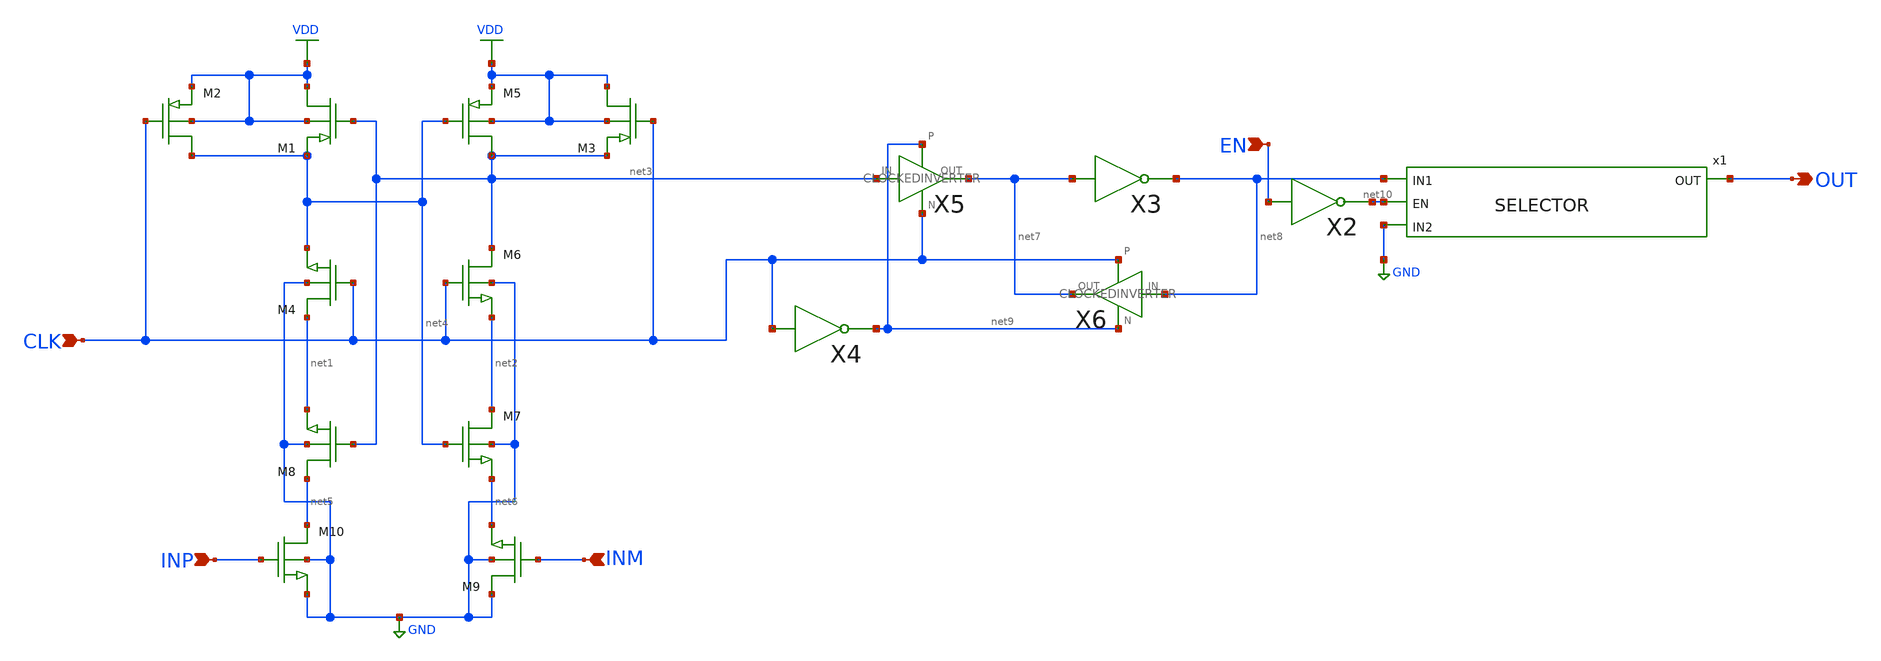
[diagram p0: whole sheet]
** sch_path: clocked_comparatorDF2.sch
**.subckt clocked_comparatorDF2 INP INM CLK OUT EN
*.ipin INP
*.ipin INM
*.ipin CLK
*.opin OUT
*.ipin EN
M4 net1 CLK net4 GND nch w=3.5u l=0.35u as=0 ps=0 ad=0 pd=0 m=1
M1 VDD net3 net4 VDD pch w=10.5u l=0.35u as=0 ps=0 ad=0 pd=0 m=1qqq
M2 net4 CLK VDD VDD pch w=10.5u l=0.35u as=0 ps=0 ad=0 pd=0 m=1
M6 net3 CLK net2 GND nch w=3.5u l=0.35u as=0 ps=0 ad=0 pd=0 m=1
M7 net2 net4 net6 GND nch w=3.5u l=0.35u as=0 ps=0 ad=0 pd=0 m=1
M8 net5 net3 net1 GND nch w=3.5u l=0.35u as=0 ps=0 ad=0 pd=0 m=1
M9 GND INM net6 GND nch w=3.5u l=0.35u as=0 ps=0 ad=0 pd=0 m=1
M10 net5 INP GND GND nch w=3.5u l=0.35u as=0 ps=0 ad=0 pd=0 m=1
M3 VDD CLK net3 VDD pch w=10.5u l=0.35u as=0 ps=0 ad=0 pd=0 m=1qqq
M5 net3 net4 VDD VDD pch w=10.5u l=0.35u as=0 ps=0 ad=0 pd=0 m=1
X3 net7 net8 INVERTER
X4 CLK net9 INVERTER
X5 net3 net7 net9 CLK CLOCKEDINVERTER
X6 net8 net7 CLK net9 CLOCKEDINVERTER
x1 net8 net10 OUT GND SELECTOR
X2 EN net10 INVERTER
**** begin user architecture code



.inc /home/tororo/LR/T_mos_model.sp

VVDD VDD 0 DC 3.3

VINP INP 0 pwl (0   0 100n 3.3 200n   0 300n 3.3 400n   0 500n 3.3 600n   0)
VINM INM 0 pwl (0 3.3 100n   0 200n 3.3 300n   0 400n 3.3 500n   0 600n 3.3)
VCLK CLK 0 pulse(0 3.3 25n 1n 1n 50n 100n)
ven EN 0 pulse(0 3.3 0n 1n 1n 200n 250n)

*Bmh mh 0 v = {u(V(EN) - 1.75)}
*Bml ml 0 v = {1 - u(V(EN) - 1.75)}
*BcurH curH 0 v = I(VVDD)*v(mh)
*BcurL curL 0 v = I(VVDD)*v(ml)

.control
tran 1n 600n
meas TRAN tplh TRIG CLK VAL=1.65 RISE=2 TARG OUT VAL=1.65 RISE=1
meas TRAN tphlen TRIG EN VAL=1.75 FALL=1 TARG OUT VAL=1.75 FALL=1
meas TRAN tphl TRIG CLK VAL=1.65 RISE=5 TARG OUT VAL=1.65 FALL=2
meas TRAN Iavg AVG I(VVDD)
*meas TRAN IavgH AVG v(curH)
*meas TRAN IavgL AVG v(curL)

plot v(OUT)
plot v(CLK)
plot v(INP)
plot v(INM)

write clocked_comparatorDF2.raw

.endc

**** end user architecture code
**.ends

* expanding   symbol:  LR/task_LATCH/INVERTER.sym # of pins=2
** sym_path: task_LATCH/INVERTER.sym
** sch_path: task_LATCH/INVERTER.sch
.subckt INVERTER IN OUT
*.opin OUT
*.ipin IN
M6 OUT IN VDD VDD pch w=10.5u l=0.35u as=0 ps=0 ad=0 pd=0 m=1
M8 OUT IN GND GND nch w=3.5u l=0.35u as=0 ps=0 ad=0 pd=0 m=1
.ends


* expanding   symbol:  LR/task_LATCH/CLOCKEDINVERTER.sym # of pins=4
** sym_path: task_LATCH/CLOCKEDINVERTER.sym
** sch_path: task_LATCH/CLOCKEDINVERTER.sch
.subckt CLOCKEDINVERTER IN OUT P N
*.opin OUT
*.ipin IN
*.ipin P
*.ipin N
M6 OUT IN net1 VDD pch w=10.5u l=0.35u as=0 ps=0 ad=0 pd=0 m=1
M8 OUT IN net2 GND nch w=3.5u l=0.35u as=0 ps=0 ad=0 pd=0 m=1
M1 net1 P VDD VDD pch w=10.5u l=0.35u as=0 ps=0 ad=0 pd=0 m=1
M2 net2 N GND GND nch w=3.5u l=0.35u as=0 ps=0 ad=0 pd=0 m=1
.ends


* expanding   symbol:  LR/task_LATCH/SELECTOR.sym # of pins=4
** sym_path: task_LATCH/SELECTOR.sym
** sch_path: task_LATCH/SELECTOR.sch
.subckt SELECTOR IN1 EN OUT IN2
*.ipin EN
*.ipin IN2
*.ipin IN1
*.opin OUT
X1 IN2 EN net2 2NANDLR
X2 IN1 net3 net1 2NANDLR
X3 net1 net2 OUT 2NANDLR
X4 EN net3 INVERTER
.ends


* expanding   symbol:  LR/task_LATCH/2NANDLR.sym # of pins=3
** sym_path: task_LATCH/2NANDLR.sym
** sch_path: task_LATCH/2NANDLR.sch
.subckt 2NANDLR A B OUT
*.ipin A
*.ipin B
*.opin OUT
M1 OUT A net1 GND nch w=3.5u l=3.5u as=0 ps=0 ad=0 pd=0 m=1
M2 OUT B VDD VDD pch w=10.5u l=3.5u as=0 ps=0 ad=0 pd=0 m=1
M3 OUT A VDD VDD pch w=10.5u l=3.5u as=0 ps=0 ad=0 pd=0 m=1
M4 net1 B GND GND nch w=3.5u l=10.5u as=0 ps=0 ad=0 pd=0 m=1
.ends

.GLOBAL VDD
.GLOBAL GND
.end
